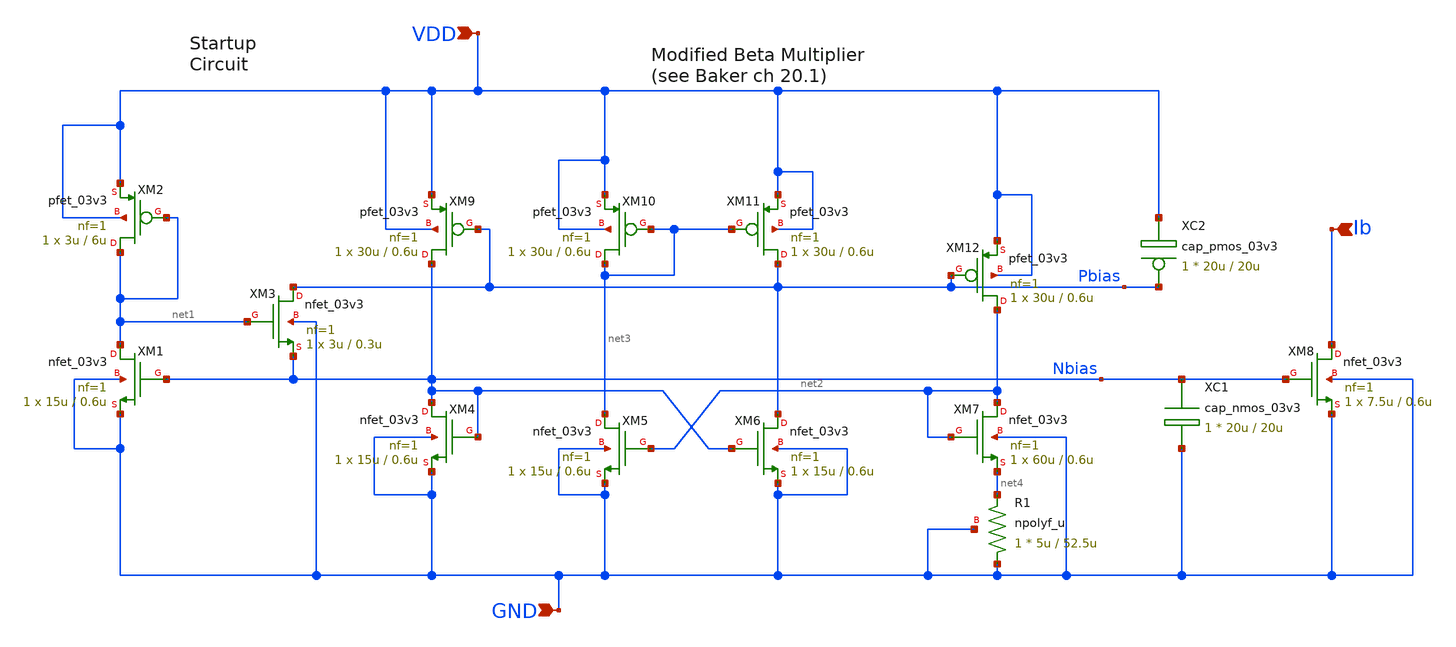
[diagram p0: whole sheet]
** sch_path: beta_mul_SC_module.sch
**.subckt beta_mul_SC_module VDD GND Ib
*.ipin VDD
*.ipin GND
*.ipin Ib
XM1 net1 Nbias GND GND nfet_03v3 L=0.6u W=15u nf=1 ad='int((nf+1)/2) * W/nf * 0.18u' as='int((nf+2)/2) * W/nf * 0.18u'
+ pd='2*int((nf+1)/2) * (W/nf + 0.18u)' ps='2*int((nf+2)/2) * (W/nf + 0.18u)' nrd='0.18u / W' nrs='0.18u / W'
+ sa=0 sb=0 sd=0 m=1 par=1
XM2 net1 net1 VDD VDD pfet_03v3 L=6u W=3u nf=1 ad='int((nf+1)/2) * W/nf * 0.18u' as='int((nf+2)/2) * W/nf * 0.18u'
+ pd='2*int((nf+1)/2) * (W/nf + 0.18u)' ps='2*int((nf+2)/2) * (W/nf + 0.18u)' nrd='0.18u / W' nrs='0.18u / W'
+ sa=0 sb=0 sd=0 m=1 par=1
XM3 Pbias net1 Nbias GND nfet_03v3 L=0.3u W=3u nf=1 ad='int((nf+1)/2) * W/nf * 0.18u' as='int((nf+2)/2) * W/nf * 0.18u'
+ pd='2*int((nf+1)/2) * (W/nf + 0.18u)' ps='2*int((nf+2)/2) * (W/nf + 0.18u)' nrd='0.18u / W' nrs='0.18u / W'
+ sa=0 sb=0 sd=0 m=1 par=1
XM4 Nbias Nbias GND GND nfet_03v3 L=0.6u W=15u nf=1 ad='int((nf+1)/2) * W/nf * 0.18u' as='int((nf+2)/2) * W/nf * 0.18u'
+ pd='2*int((nf+1)/2) * (W/nf + 0.18u)' ps='2*int((nf+2)/2) * (W/nf + 0.18u)' nrd='0.18u / W' nrs='0.18u / W'
+ sa=0 sb=0 sd=0 m=1 par=1
XM5 net3 net2 GND GND nfet_03v3 L=0.6u W=15u nf=1 ad='int((nf+1)/2) * W/nf * 0.18u' as='int((nf+2)/2) * W/nf * 0.18u'
+ pd='2*int((nf+1)/2) * (W/nf + 0.18u)' ps='2*int((nf+2)/2) * (W/nf + 0.18u)' nrd='0.18u / W' nrs='0.18u / W'
+ sa=0 sb=0 sd=0 m=1 par=1
XM6 Pbias Nbias GND GND nfet_03v3 L=0.6u W=15u nf=1 ad='int((nf+1)/2) * W/nf * 0.18u' as='int((nf+2)/2) * W/nf * 0.18u'
+ pd='2*int((nf+1)/2) * (W/nf + 0.18u)' ps='2*int((nf+2)/2) * (W/nf + 0.18u)' nrd='0.18u / W' nrs='0.18u / W'
+ sa=0 sb=0 sd=0 m=1 par=1
XM7 net2 net2 net4 GND nfet_03v3 L=0.6u W=60u nf=1 ad='int((nf+1)/2) * W/nf * 0.18u' as='int((nf+2)/2) * W/nf * 0.18u'
+ pd='2*int((nf+1)/2) * (W/nf + 0.18u)' ps='2*int((nf+2)/2) * (W/nf + 0.18u)' nrd='0.18u / W' nrs='0.18u / W'
+ sa=0 sb=0 sd=0 m=1 par=1
XM9 Nbias Pbias VDD VDD pfet_03v3 L=0.6u W=30u nf=1 ad='int((nf+1)/2) * W/nf * 0.18u' as='int((nf+2)/2) * W/nf * 0.18u'
+ pd='2*int((nf+1)/2) * (W/nf + 0.18u)' ps='2*int((nf+2)/2) * (W/nf + 0.18u)' nrd='0.18u / W' nrs='0.18u / W'
+ sa=0 sb=0 sd=0 m=1 par=1
XM10 net3 net3 VDD VDD pfet_03v3 L=0.6u W=30u nf=1 ad='int((nf+1)/2) * W/nf * 0.18u' as='int((nf+2)/2) * W/nf * 0.18u'
+ pd='2*int((nf+1)/2) * (W/nf + 0.18u)' ps='2*int((nf+2)/2) * (W/nf + 0.18u)' nrd='0.18u / W' nrs='0.18u / W'
+ sa=0 sb=0 sd=0 m=1 par=1
XM11 Pbias net3 VDD VDD pfet_03v3 L=0.6u W=30u nf=1 ad='int((nf+1)/2) * W/nf * 0.18u' as='int((nf+2)/2) * W/nf * 0.18u'
+ pd='2*int((nf+1)/2) * (W/nf + 0.18u)' ps='2*int((nf+2)/2) * (W/nf + 0.18u)' nrd='0.18u / W' nrs='0.18u / W'
+ sa=0 sb=0 sd=0 m=1 par=1
XM12 net2 Pbias VDD VDD pfet_03v3 L=0.6u W=30u nf=1 ad='int((nf+1)/2) * W/nf * 0.18u' as='int((nf+2)/2) * W/nf * 0.18u'
+ pd='2*int((nf+1)/2) * (W/nf + 0.18u)' ps='2*int((nf+2)/2) * (W/nf + 0.18u)' nrd='0.18u / W' nrs='0.18u / W'
+ sa=0 sb=0 sd=0 m=1 par=1
XM8 Ib Nbias GND GND nfet_03v3 L=0.6u W=7.5u nf=1 ad='int((nf+1)/2) * W/nf * 0.18u' as='int((nf+2)/2) * W/nf * 0.18u'
+ pd='2*int((nf+1)/2) * (W/nf + 0.18u)' ps='2*int((nf+2)/2) * (W/nf + 0.18u)' nrd='0.18u / W' nrs='0.18u / W'
+ sa=0 sb=0 sd=0 m=1 par=1
XC1 Nbias GND cap_nmos_03v3 c_width=20u c_length=20u m=1
XC2 Pbias VDD cap_pmos_03v3 c_width=20u c_length=20u m=1
XR1 GND net4 GND npolyf_u r_width=5u r_length=52.5u m=1
**.ends
.end
